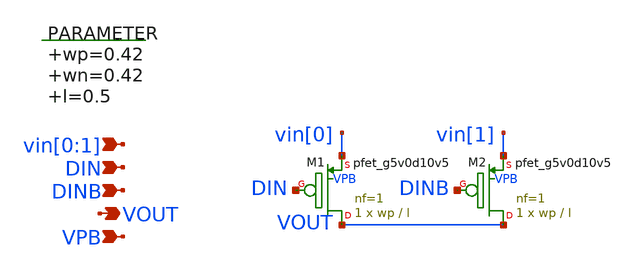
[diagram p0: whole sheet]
** sch_path: xschem/switch_pmos_2g_1o.sch
**.subckt switch_pmos_2g_1o vin[0],vin[1] VOUT VPB DIN DINB
*.ipin vin[0],vin[1]
*.opin VOUT
*.ipin VPB
*.ipin DIN
*.ipin DINB
.param wp=0.42 wn=0.42 l=0.5

XM1 VOUT DIN vin[0] VPB sky130_fd_pr__pfet_g5v0d10v5 L=l W=wp nf=1 ad='int((nf+1)/2) * W/nf * 0.29' as='int((nf+2)/2) * W/nf * 0.29'
+ pd='2*int((nf+1)/2) * (W/nf + 0.29)' ps='2*int((nf+2)/2) * (W/nf + 0.29)' nrd='0.29 / W' nrs='0.29 / W'
+ sa=0 sb=0 sd=0 mult=1 m=1
XM2 VOUT DINB vin[1] VPB sky130_fd_pr__pfet_g5v0d10v5 L=l W=wp nf=1 ad='int((nf+1)/2) * W/nf * 0.29'
+ as='int((nf+2)/2) * W/nf * 0.29' pd='2*int((nf+1)/2) * (W/nf + 0.29)' ps='2*int((nf+2)/2) * (W/nf + 0.29)'
+ nrd='0.29 / W' nrs='0.29 / W' sa=0 sb=0 sd=0 mult=1 m=1
**.ends
.end
